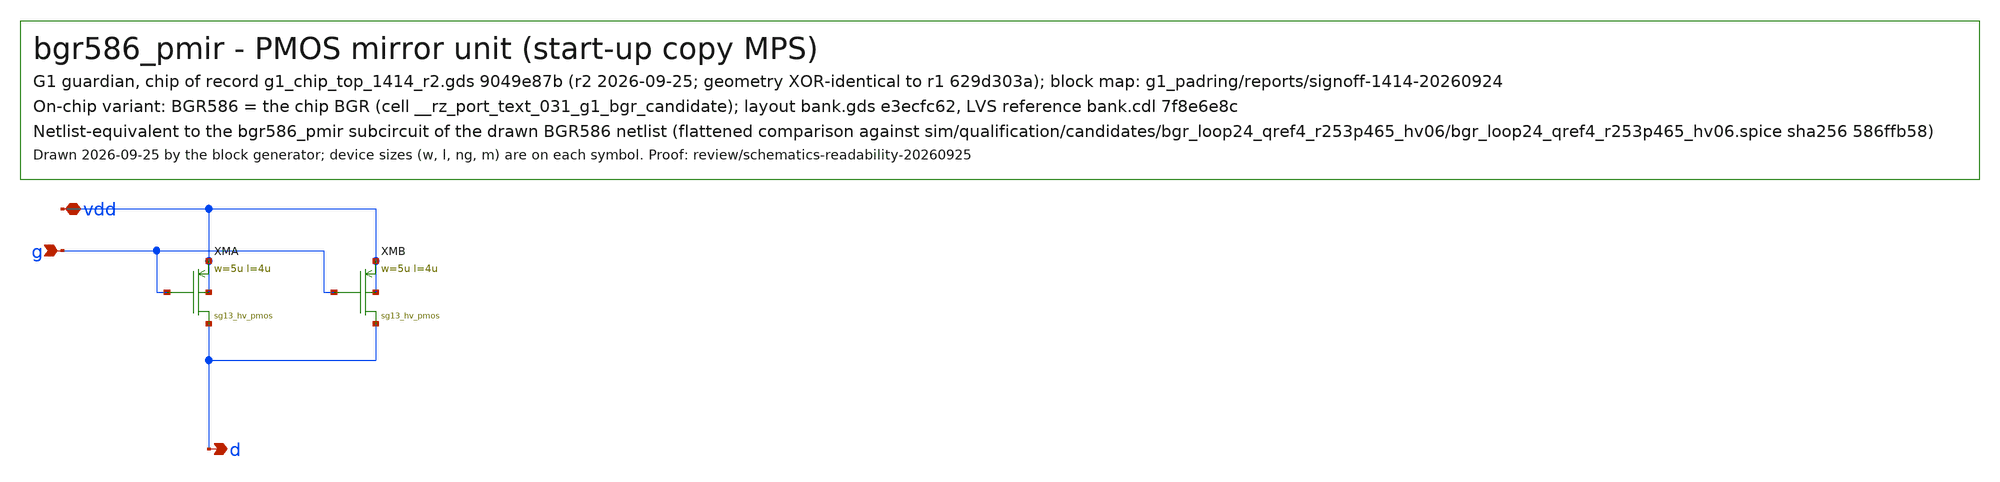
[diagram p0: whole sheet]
** sch_path: designs/g1-guardian/blocks/g1_bgr/xschem/bgr586/bgr586_pmir.sch
**.subckt bgr586_pmir d g vdd
*.opin d
*.ipin g
*.iopin vdd
XMA d g vdd vdd sg13_hv_pmos l=4u w=5u as=1.7p ad=1.7p ps=10.68u pd=10.68u rfmode=0
XMB d g vdd vdd sg13_hv_pmos l=4u w=5u as=1.7p ad=1.7p ps=10.68u pd=10.68u rfmode=0
**.ends
.end
